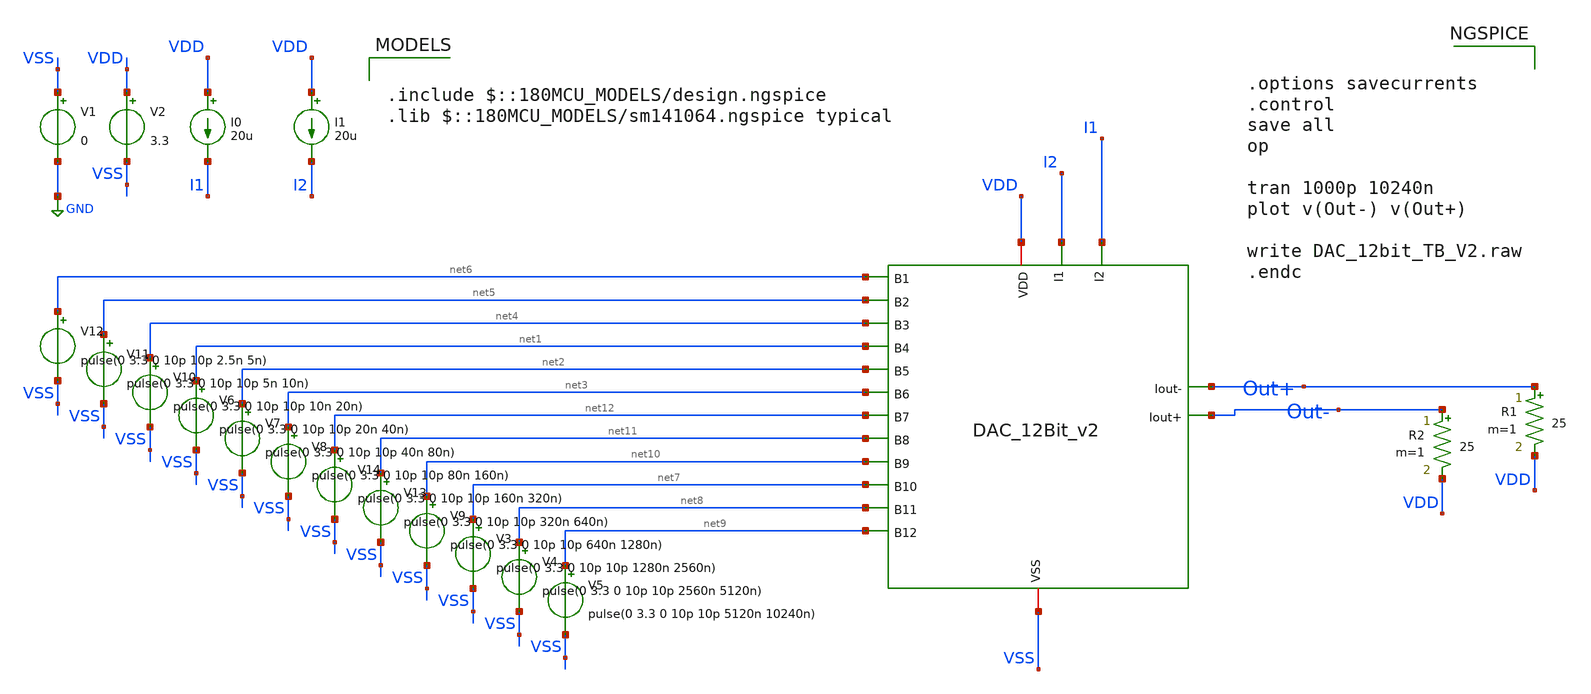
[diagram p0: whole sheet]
** sch_path: DAC_PAKISTAN_01/Pakistan1_Xschem/DAC_12bit_TB_V2.sch
**.subckt DAC_12bit_TB_V2
V1 VSS GND 0
V2 VDD VSS 3.3
V6 net1 VSS pulse(0 3.3 0 10p 10p 20n 40n)
V7 net2 VSS pulse(0 3.3 0 10p 10p 40n 80n)
V8 net3 VSS pulse(0 3.3 0 10p 10p 80n 160n)
V10 net4 VSS pulse(0 3.3 0 10p 10p 10n 20n)
V11 net5 VSS pulse(0 3.3 0 10p 10p 5n 10n)
V12 net6 VSS pulse(0 3.3 0 10p 10p 2.5n 5n)
I0 VDD I1 20u
V3 net7 VSS pulse(0 3.3 0 10p 10p 1280n 2560n)
V4 net8 VSS pulse(0 3.3 0 10p 10p 2560n 5120n)
V5 net9 VSS pulse(0 3.3 0 10p 10p 5120n 10240n)
V9 net10 VSS pulse(0 3.3 0 10p 10p 640n 1280n)
V13 net11 VSS pulse(0 3.3 0 10p 10p 320n 640n)
V14 net12 VSS pulse(0 3.3 0 10p 10p 160n 320n)
I1 VDD I2 20u
R1 Out+ VDD 25 m=1
R2 Out- VDD 25 m=1
x1 net2 net10 VDD I2 net8 net6 net12 Out+ net4 net9 net7 net1 net11 Out- I1 net3 net5 VSS
+ DAC_12Bit_V2
**** begin user architecture code

.include $::180MCU_MODELS/design.ngspice
.lib $::180MCU_MODELS/sm141064.ngspice typical



.options savecurrents
.control
save all
op

tran 1000p 10240n
plot v(Out-) v(Out+)

write DAC_12bit_TB_V2.raw
.endc


**** end user architecture code
**.ends
.GLOBAL GND
.end
